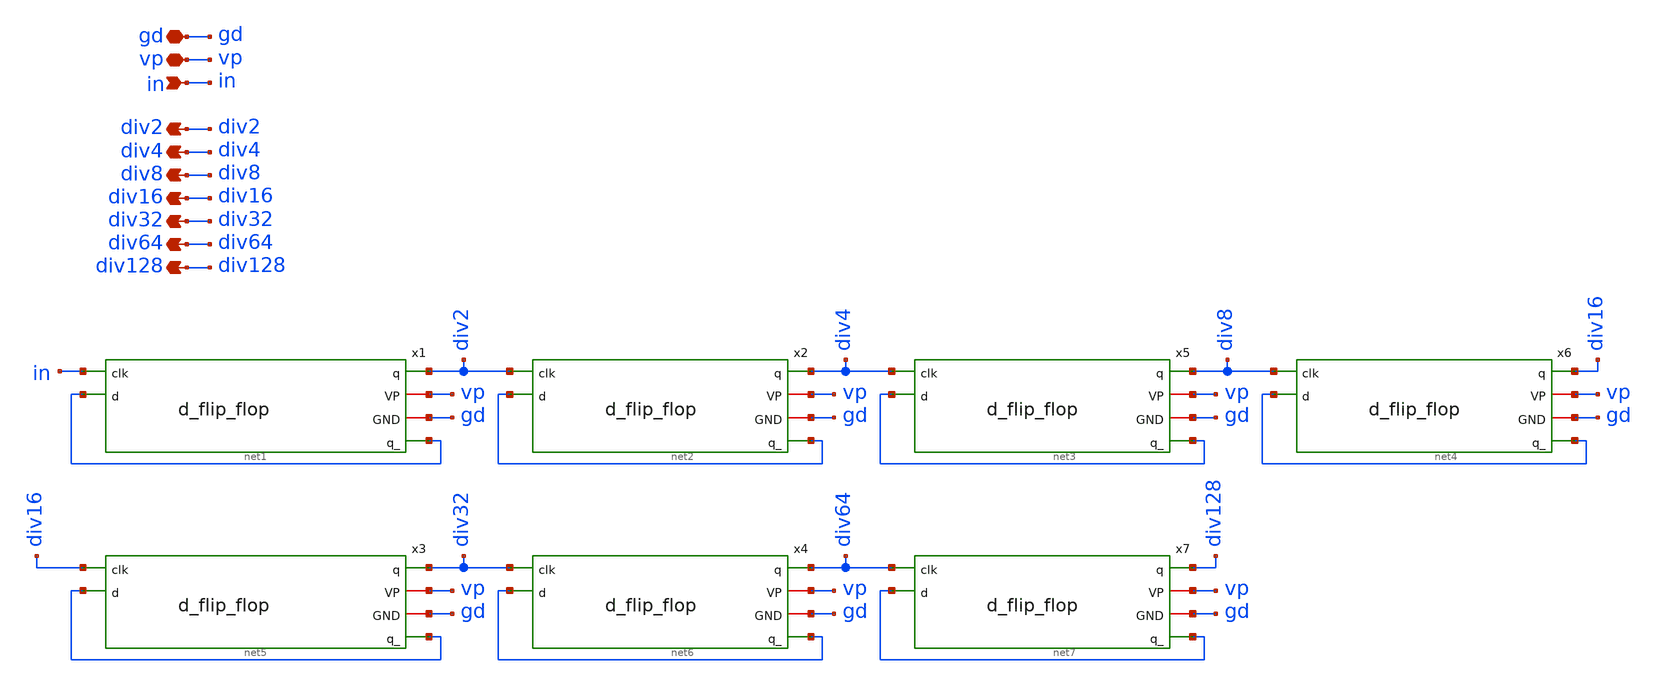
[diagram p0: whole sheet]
** sch_path: PLL0663-main/schematic/xschem/divider/2Div.sch
**.subckt 2Div gd in vp div2 div4 div8 div16 div32 div64 div128
*.iopin gd
*.ipin in
*.iopin vp
*.opin div2
*.opin div4
*.opin div8
*.opin div16
*.opin div32
*.opin div64
*.opin div128
x3 div32 vp gd net5 div16 net5 d_flip_flop
x4 div64 vp gd net6 div32 net6 d_flip_flop
x7 div128 vp gd net7 div64 net7 d_flip_flop
x1 div2 vp gd net1 in net1 d_flip_flop
x2 div4 vp gd net2 div2 net2 d_flip_flop
x5 div8 vp gd net3 div4 net3 d_flip_flop
x6 div16 vp gd net4 div8 net4 d_flip_flop
**.ends
.end
